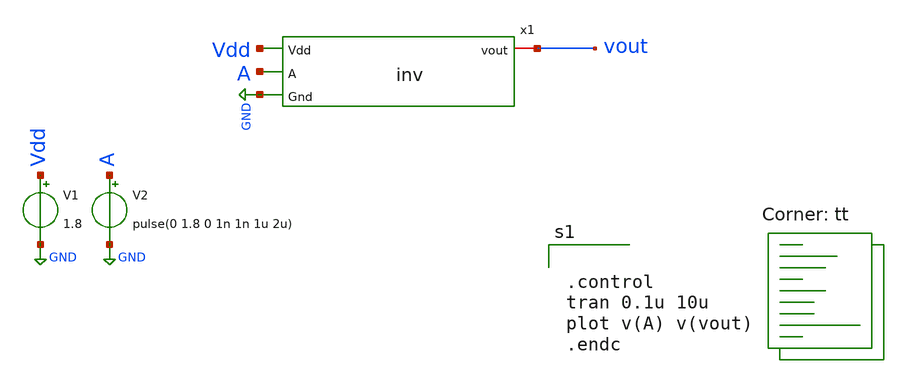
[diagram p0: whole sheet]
** sch_path: untitled.sch
**.subckt untitled
x1 Vdd vout A GND inv
V1 Vdd GND 1.8
V2 A GND pulse(0 1.8 0 1n 1n 1u 2u)
**** begin user architecture code
.lib $::SKYWATER_MODELS/sky130.lib.spice tt


.control
tran 0.1u 10u
plot v(A) v(vout)
.endc


**** end user architecture code
**.ends

* expanding   symbol:  inv.sym # of pins=4
** sym_path: inv.sym
** sch_path: inv.sch
.subckt inv Vdd vout A Gnd
*.iopin vout
*.ipin A
*.ipin Vdd
*.ipin Gnd
XM1 vout A Gnd Gnd sky130_fd_pr__nfet_01v8 L=0.15 W=1 nf=1 ad='int((1 + 1)/2) * 1 / 1 * 0.29' as='int((1 + 2)/2) * 1 / 1 * 0.29'
+ pd='2*int((1 + 1)/2) * (1 / 1 + 0.29)' ps='2*int((1 + 2)/2) * (1 / 1 + 0.29)' nrd='0.29 / 1 ' nrs='0.29 / 1 '
+ sa=0 sb=0 sd=0 mult=1 m=1
XM2 vout A Vdd Vdd sky130_fd_pr__pfet_01v8 L=0.15 W='1 * 1 ' nf=1 ad='int((1 + 1)/2) * 1 / 1 * 0.29'
+ as='int((1 + 2)/2) * 1 / 1 * 0.29' pd='2*int((1 + 1)/2) * (1 / 1 + 0.29)' ps='2*int((1 + 2)/2) * (1 / 1 + 0.29)'
+ nrd='0.29 / 1 ' nrs='0.29 / 1 ' sa=0 sb=0 sd=0 mult=1 m=1
.ends

.GLOBAL GND
.end
